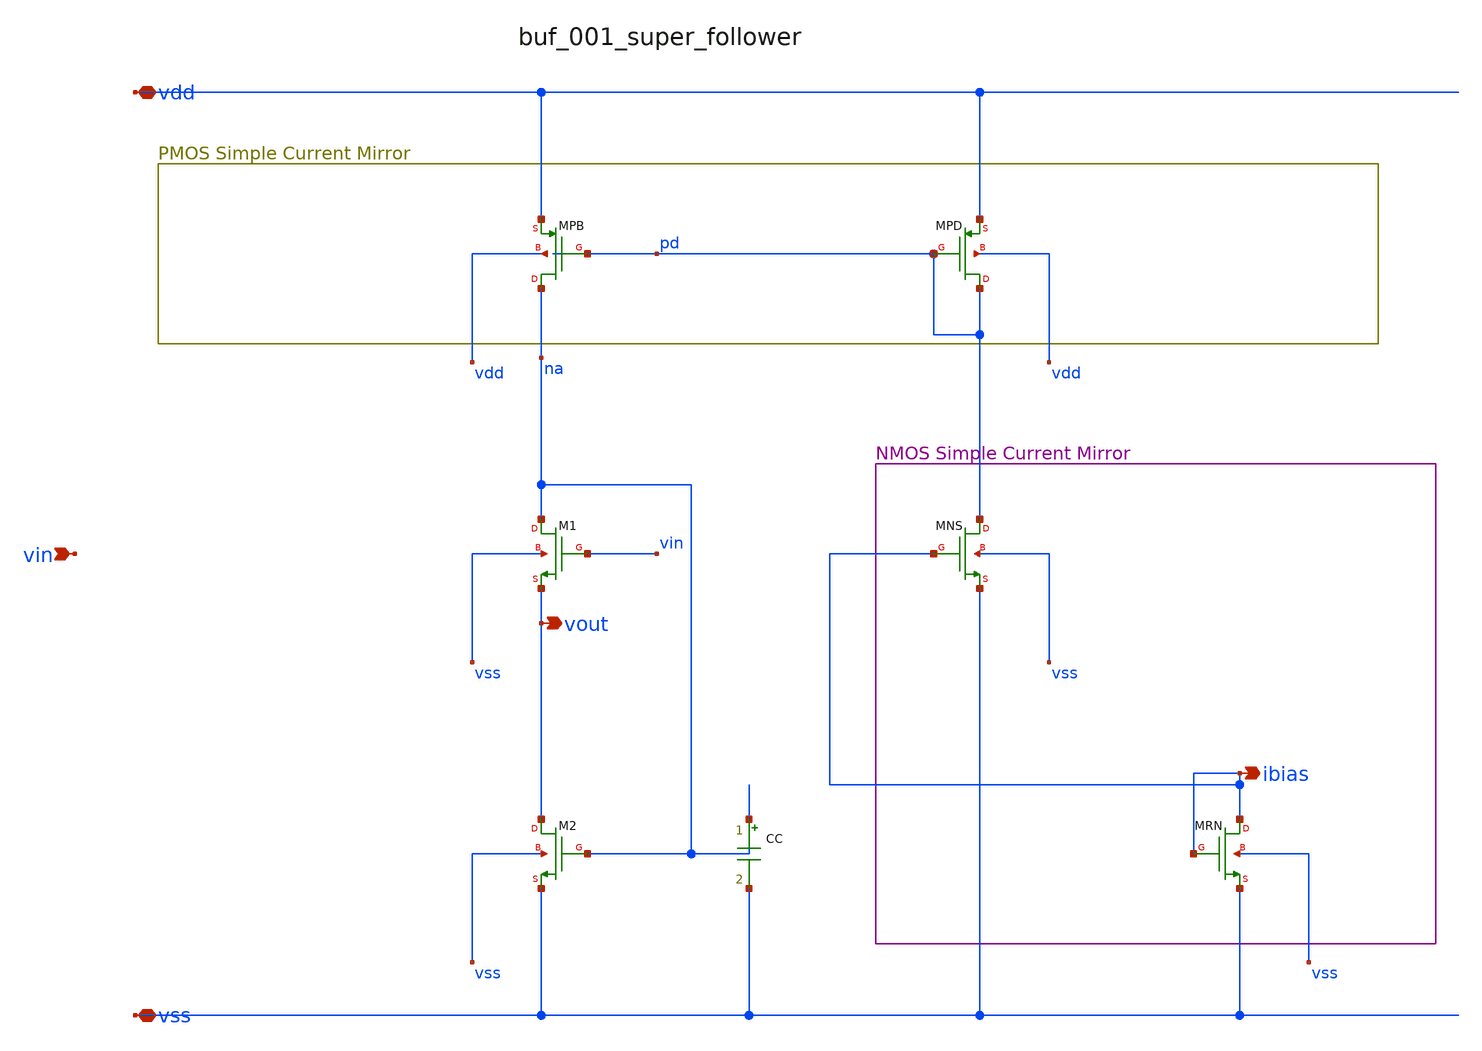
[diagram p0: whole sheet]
** sch_path: analog-db/raw/buf_001_super_follower/buf_001_super_follower_annotated.sch
**.subckt buf_001_super_follower_annotated vdd vss ibias vout vin
*.iopin vdd
*.iopin vss
*.opin ibias
*.opin vout
*.ipin vin
CC na vss x_cc m=1
XM1 na vin vout vss sg13_lv_nmos w=x_dut_xm1_w l=x_dut_xm1_l ng=1 m=x_dut_xm1_m
XM2 vout na vss vss sg13_lv_nmos w=x_dut_xm2_w l=x_dut_xm2_l ng=1 m=x_dut_xm2_m
XMNS pd ibias vss vss sg13_lv_nmos w=x_dut_xmns_w l=x_dut_xmns_l ng=1 m=x_dut_xmns_m
XMPB na pd vdd vdd sg13_lv_pmos w=x_dut_xmpb_w l=x_dut_xmpb_l ng=1 m=x_dut_xmpb_m
XMPD pd pd vdd vdd sg13_lv_pmos w=x_dut_xmpd_w l=x_dut_xmpd_l ng=1 m=x_dut_xmpd_m
XMRN ibias ibias vss vss sg13_lv_nmos w=x_dut_xmrn_w l=x_dut_xmrn_l ng=1 m=x_dut_xmrn_m
**.ends
.end
